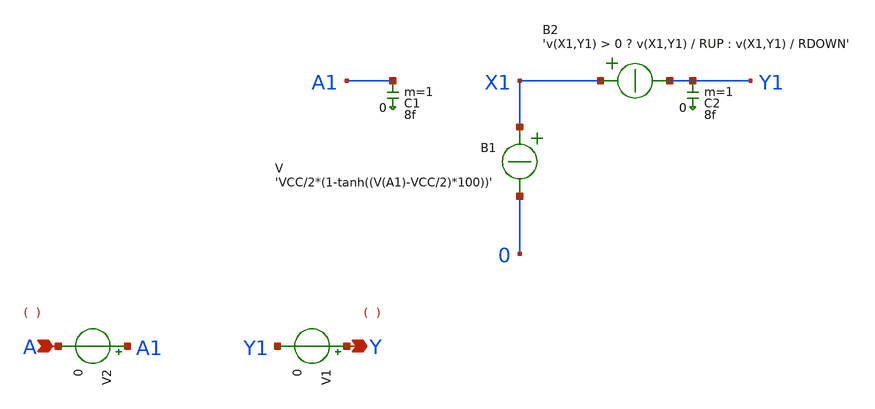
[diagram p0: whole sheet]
** sch_path: xschem_libs_newsym/ngspice/inv_ngspice/schematic/inv_ngspice.sch
* Copyright (C) 1998-2024 Stefan Frederik Schippers
* This program is free software; you can redistribute it and/or modify
* it under the terms of the GNU General Public License as published by
* the Free Software Foundation; either version 2 of the License, or
* (at your option) any later version.
* This program is distributed in the hope that it will be useful,
* but WITHOUT ANY WARRANTY; without even the implied warranty of
* MERCHANTABILITY or FITNESS FOR A PARTICULAR PURPOSE.  See the
* GNU General Public License for more details.
* You should have received a copy of the GNU General Public License
* along with this program; if not, write to the Free Software
**.subckt inv_ngspice A Y
*.ipin A
*.opin Y
B1 X1 0 V = 'VCC/2*(1-tanh((V(A1)-VCC/2)*100))'
C1 A1 0 8f m=1
C2 Y1 0 8f m=1
V1 Y Y1 0
.save i(v1)
V2 A1 A 0
.save i(v2)
B2 X1 Y1 I = 'v(X1,Y1) > 0 ? v(X1,Y1) / RUP : v(X1,Y1) / RDOWN'
**.ends
.end
